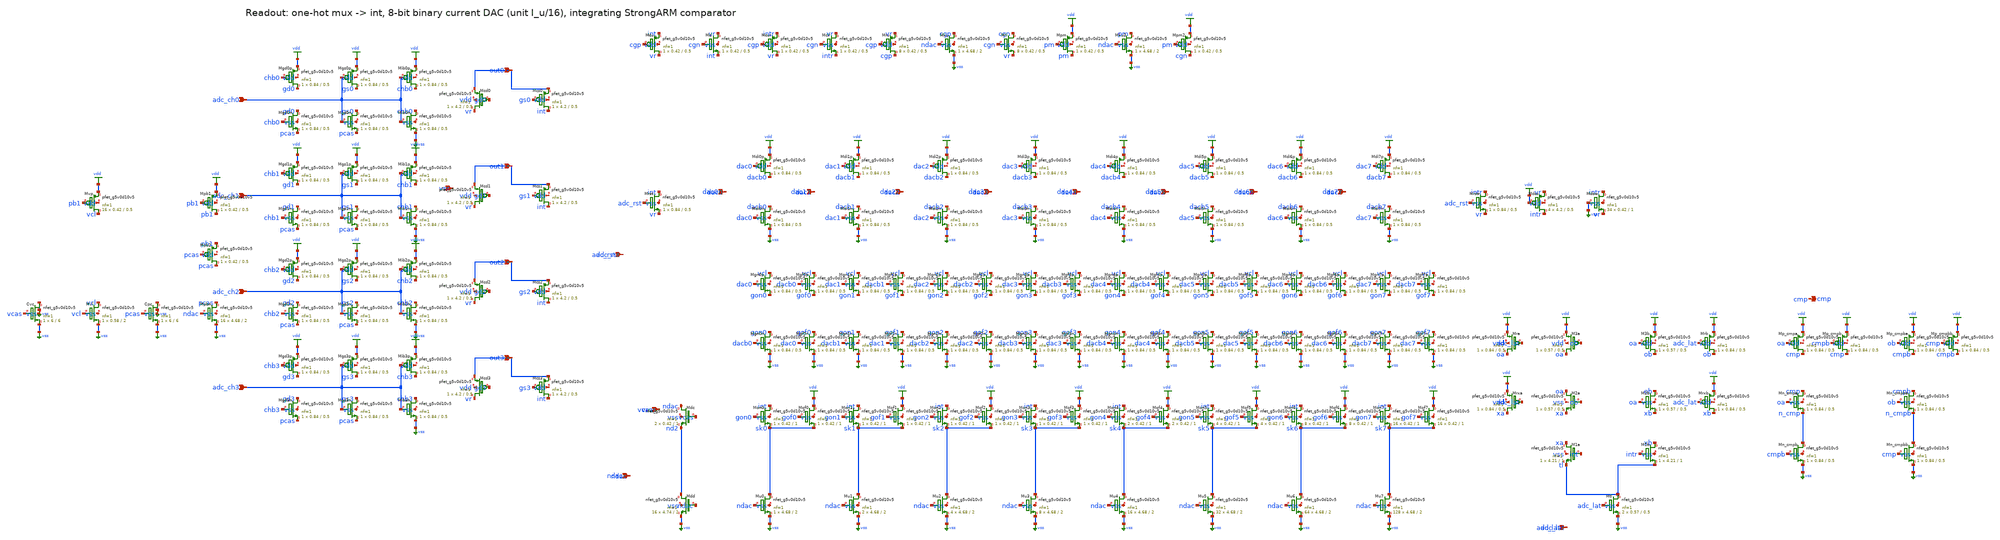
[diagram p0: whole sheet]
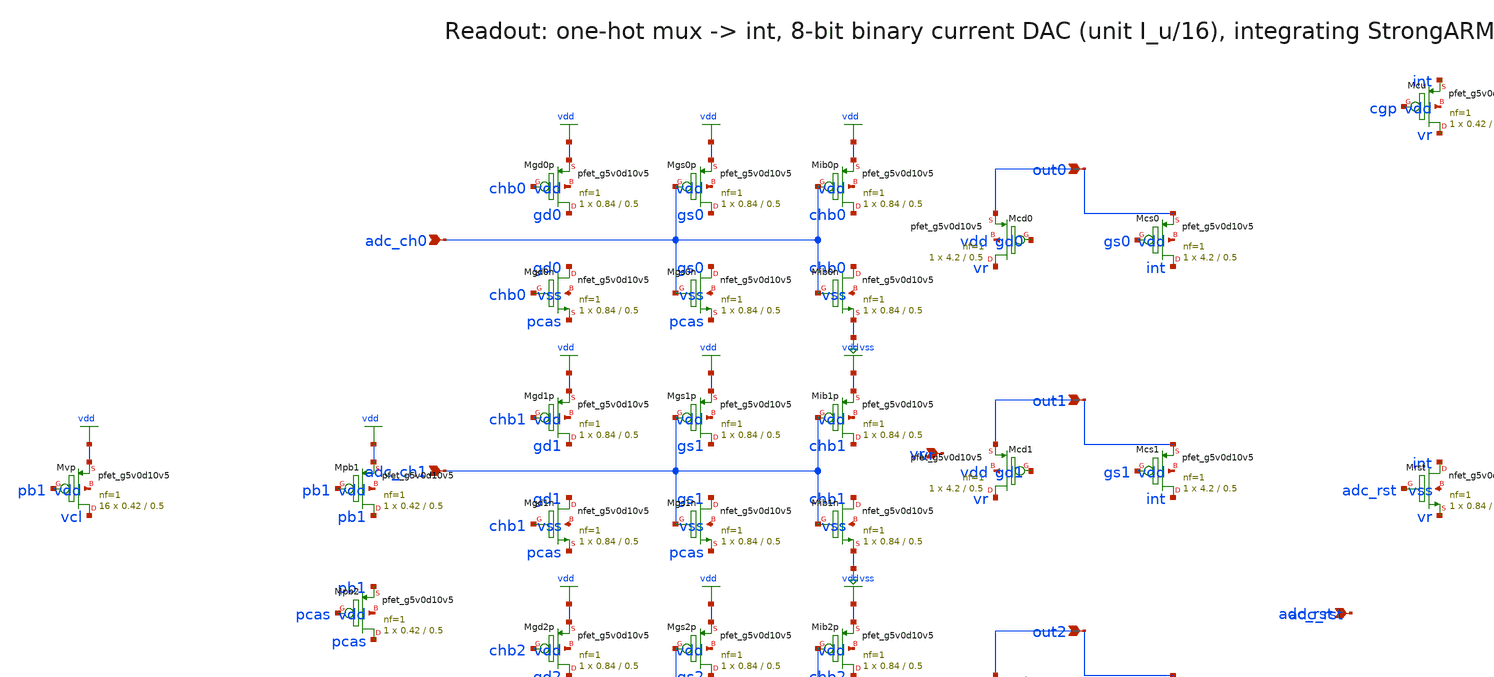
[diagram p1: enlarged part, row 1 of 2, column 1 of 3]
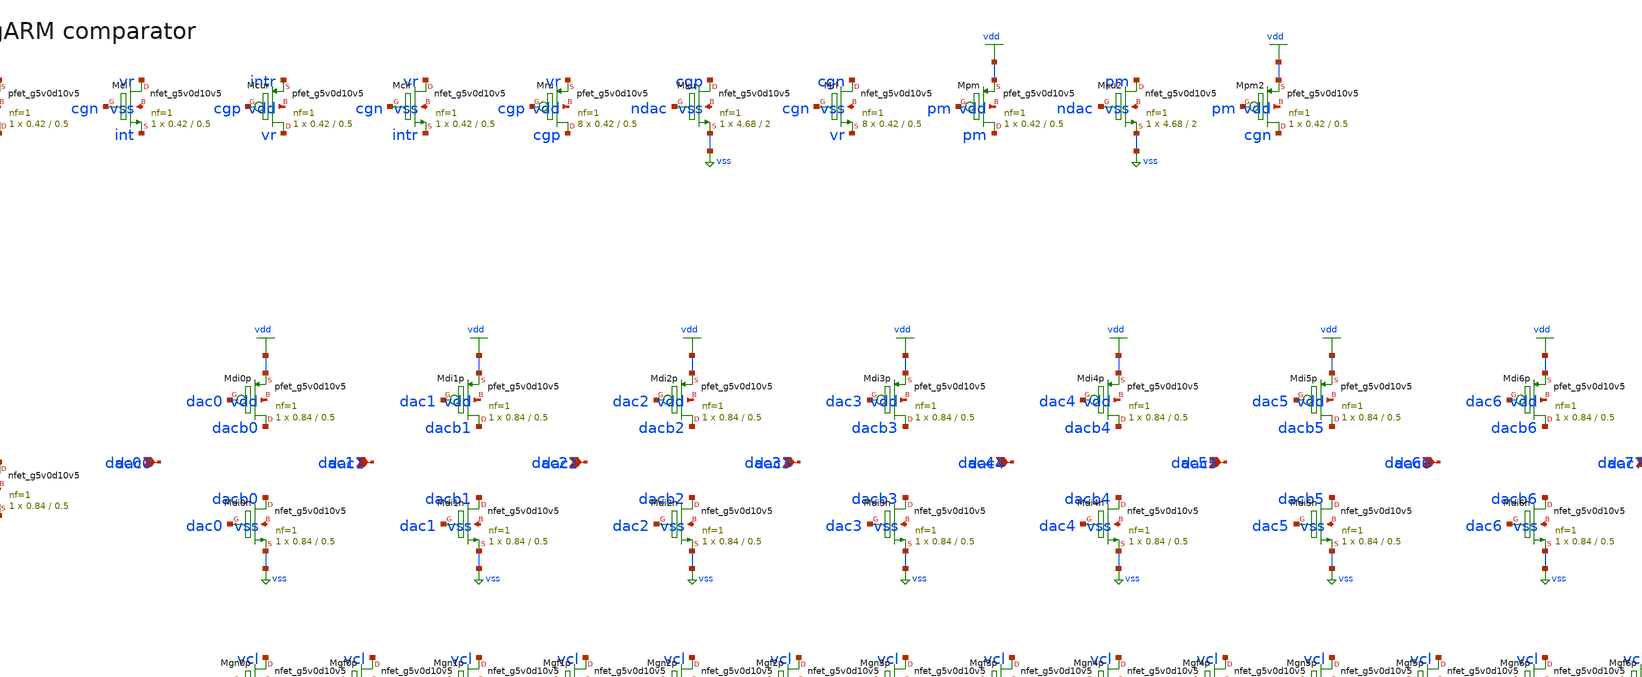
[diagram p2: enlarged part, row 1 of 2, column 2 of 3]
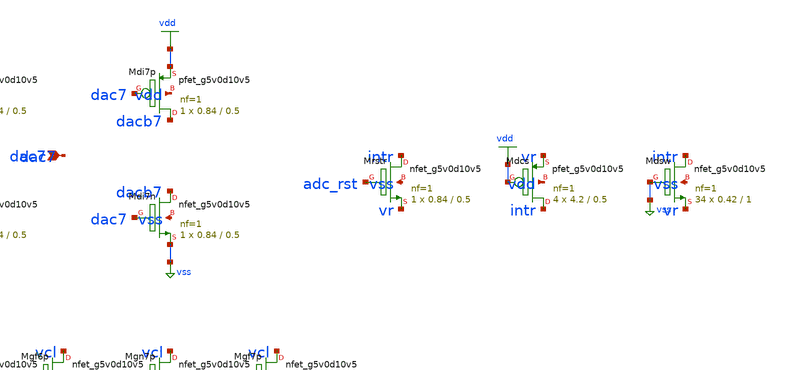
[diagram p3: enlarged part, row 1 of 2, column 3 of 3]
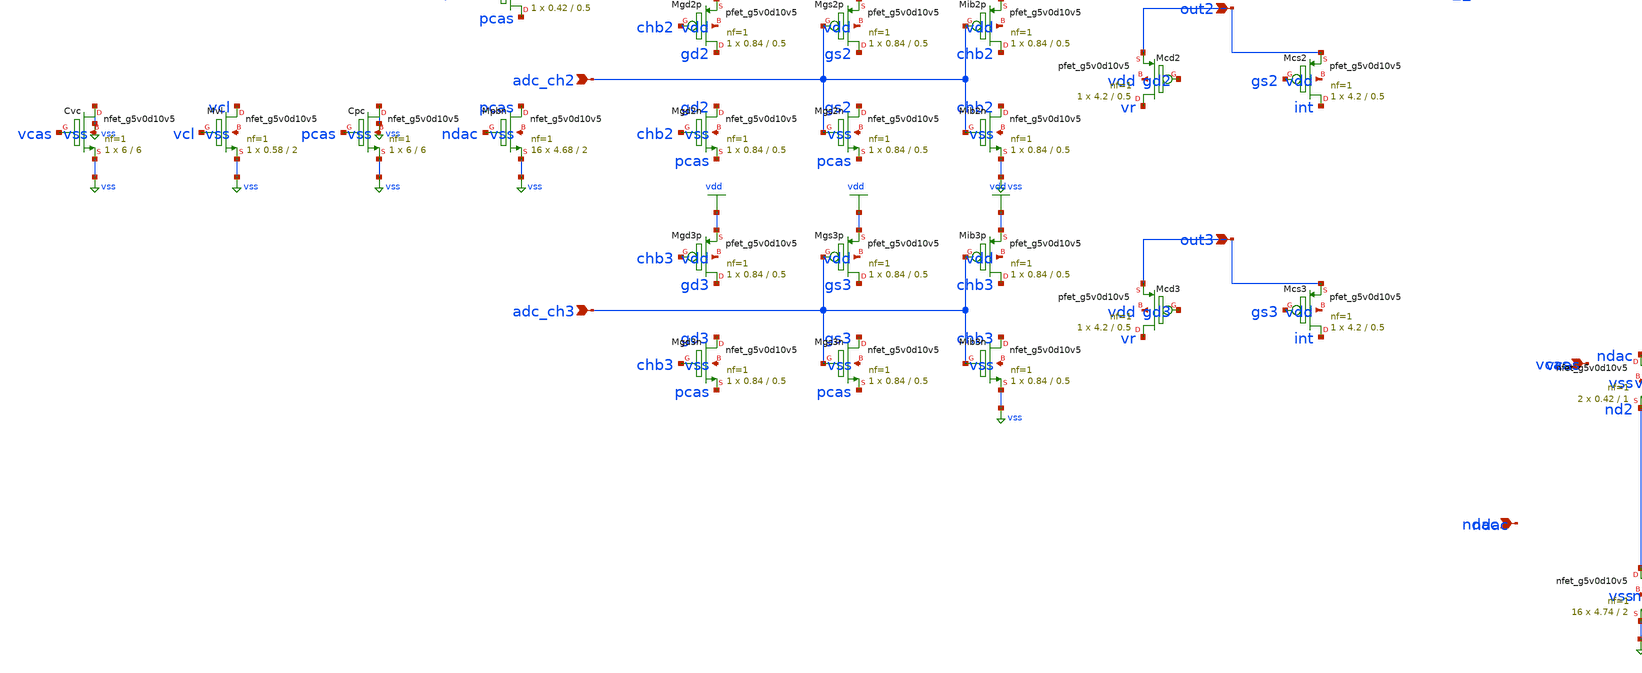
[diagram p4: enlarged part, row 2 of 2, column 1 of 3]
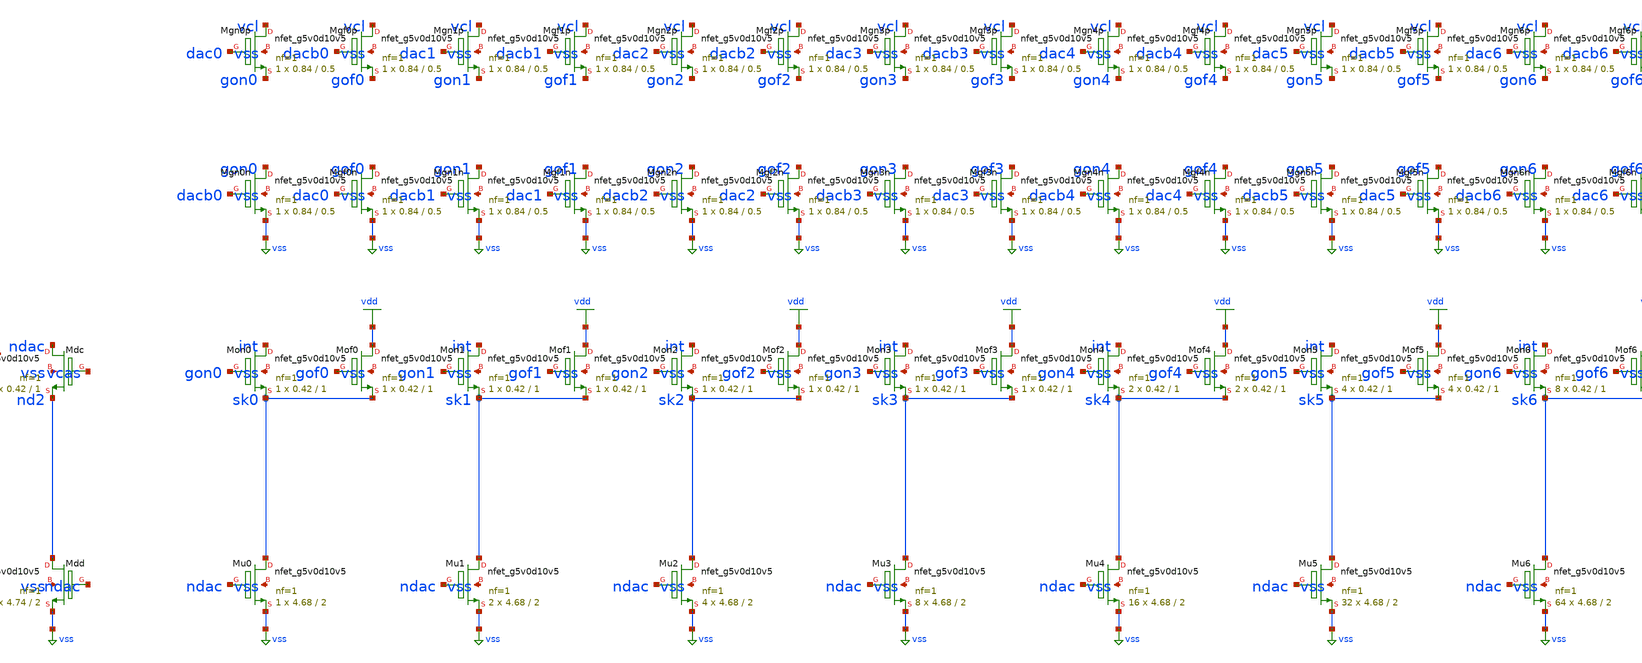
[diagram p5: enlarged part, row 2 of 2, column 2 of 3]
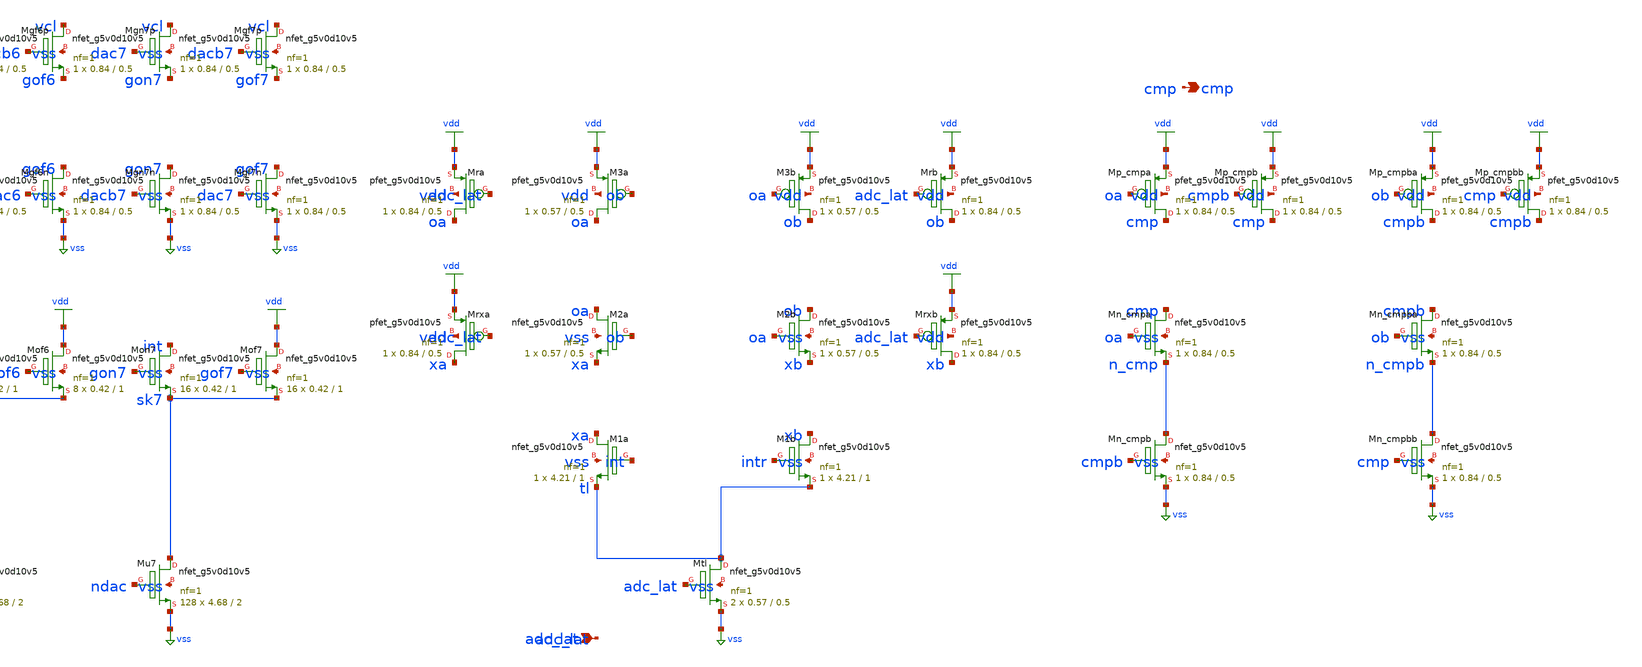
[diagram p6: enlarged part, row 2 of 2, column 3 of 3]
** sch_path: xschem/rt5w_readout.sch
**.subckt rt5w_readout out0 adc_ch0 out1 adc_ch1 out2 adc_ch2 out3 adc_ch3 dac0 dac1 dac2 dac3 dac4
*+ dac5 dac6 dac7 ndac vcas vr adc_rst adc_lat cmp
*.ipin out0
*.ipin adc_ch0
*.ipin out1
*.ipin adc_ch1
*.ipin out2
*.ipin adc_ch2
*.ipin out3
*.ipin adc_ch3
*.ipin dac0
*.ipin dac1
*.ipin dac2
*.ipin dac3
*.ipin dac4
*.ipin dac5
*.ipin dac6
*.ipin dac7
*.ipin ndac
*.ipin vcas
*.ipin vr
*.ipin adc_rst
*.ipin adc_lat
*.opin cmp
XMcs0 int gs0 out0 vdd sky130_fd_pr__pfet_g5v0d10v5 L=0.5 W=4.2 nf=1 ad=1.218 as=1.218 pd=8.98
+ ps=8.98 nrd=0.06905 nrs=0.06905 sa=0 sb=0 sd=0 mult=1 m=1
XMcd0 vr gd0 out0 vdd sky130_fd_pr__pfet_g5v0d10v5 L=0.5 W=4.2 nf=1 ad=1.218 as=1.218 pd=8.98
+ ps=8.98 nrd=0.06905 nrs=0.06905 sa=0 sb=0 sd=0 mult=1 m=1
XMib0p chb0 adc_ch0 vdd vdd sky130_fd_pr__pfet_g5v0d10v5 L=0.5 W=0.84 nf=1 ad=0.2436 as=0.2436
+ pd=2.26 ps=2.26 nrd=0.3452 nrs=0.3452 sa=0 sb=0 sd=0 mult=1 m=1
XMib0n chb0 adc_ch0 vss vss sky130_fd_pr__nfet_g5v0d10v5 L=0.5 W=0.84 nf=1 ad=0.2436 as=0.2436
+ pd=2.26 ps=2.26 nrd=0.3452 nrs=0.3452 sa=0 sb=0 sd=0 mult=1 m=1
XMgs0p gs0 adc_ch0 vdd vdd sky130_fd_pr__pfet_g5v0d10v5 L=0.5 W=0.84 nf=1 ad=0.2436 as=0.2436
+ pd=2.26 ps=2.26 nrd=0.3452 nrs=0.3452 sa=0 sb=0 sd=0 mult=1 m=1
XMgs0n gs0 adc_ch0 pcas vss sky130_fd_pr__nfet_g5v0d10v5 L=0.5 W=0.84 nf=1 ad=0.2436 as=0.2436
+ pd=2.26 ps=2.26 nrd=0.3452 nrs=0.3452 sa=0 sb=0 sd=0 mult=1 m=1
XMgd0p gd0 chb0 vdd vdd sky130_fd_pr__pfet_g5v0d10v5 L=0.5 W=0.84 nf=1 ad=0.2436 as=0.2436 pd=2.26
+ ps=2.26 nrd=0.3452 nrs=0.3452 sa=0 sb=0 sd=0 mult=1 m=1
XMgd0n gd0 chb0 pcas vss sky130_fd_pr__nfet_g5v0d10v5 L=0.5 W=0.84 nf=1 ad=0.2436 as=0.2436 pd=2.26
+ ps=2.26 nrd=0.3452 nrs=0.3452 sa=0 sb=0 sd=0 mult=1 m=1
XMcs1 int gs1 out1 vdd sky130_fd_pr__pfet_g5v0d10v5 L=0.5 W=4.2 nf=1 ad=1.218 as=1.218 pd=8.98
+ ps=8.98 nrd=0.06905 nrs=0.06905 sa=0 sb=0 sd=0 mult=1 m=1
XMcd1 vr gd1 out1 vdd sky130_fd_pr__pfet_g5v0d10v5 L=0.5 W=4.2 nf=1 ad=1.218 as=1.218 pd=8.98
+ ps=8.98 nrd=0.06905 nrs=0.06905 sa=0 sb=0 sd=0 mult=1 m=1
XMib1p chb1 adc_ch1 vdd vdd sky130_fd_pr__pfet_g5v0d10v5 L=0.5 W=0.84 nf=1 ad=0.2436 as=0.2436
+ pd=2.26 ps=2.26 nrd=0.3452 nrs=0.3452 sa=0 sb=0 sd=0 mult=1 m=1
XMib1n chb1 adc_ch1 vss vss sky130_fd_pr__nfet_g5v0d10v5 L=0.5 W=0.84 nf=1 ad=0.2436 as=0.2436
+ pd=2.26 ps=2.26 nrd=0.3452 nrs=0.3452 sa=0 sb=0 sd=0 mult=1 m=1
XMgs1p gs1 adc_ch1 vdd vdd sky130_fd_pr__pfet_g5v0d10v5 L=0.5 W=0.84 nf=1 ad=0.2436 as=0.2436
+ pd=2.26 ps=2.26 nrd=0.3452 nrs=0.3452 sa=0 sb=0 sd=0 mult=1 m=1
XMgs1n gs1 adc_ch1 pcas vss sky130_fd_pr__nfet_g5v0d10v5 L=0.5 W=0.84 nf=1 ad=0.2436 as=0.2436
+ pd=2.26 ps=2.26 nrd=0.3452 nrs=0.3452 sa=0 sb=0 sd=0 mult=1 m=1
XMgd1p gd1 chb1 vdd vdd sky130_fd_pr__pfet_g5v0d10v5 L=0.5 W=0.84 nf=1 ad=0.2436 as=0.2436 pd=2.26
+ ps=2.26 nrd=0.3452 nrs=0.3452 sa=0 sb=0 sd=0 mult=1 m=1
XMgd1n gd1 chb1 pcas vss sky130_fd_pr__nfet_g5v0d10v5 L=0.5 W=0.84 nf=1 ad=0.2436 as=0.2436 pd=2.26
+ ps=2.26 nrd=0.3452 nrs=0.3452 sa=0 sb=0 sd=0 mult=1 m=1
XMcs2 int gs2 out2 vdd sky130_fd_pr__pfet_g5v0d10v5 L=0.5 W=4.2 nf=1 ad=1.218 as=1.218 pd=8.98
+ ps=8.98 nrd=0.06905 nrs=0.06905 sa=0 sb=0 sd=0 mult=1 m=1
XMcd2 vr gd2 out2 vdd sky130_fd_pr__pfet_g5v0d10v5 L=0.5 W=4.2 nf=1 ad=1.218 as=1.218 pd=8.98
+ ps=8.98 nrd=0.06905 nrs=0.06905 sa=0 sb=0 sd=0 mult=1 m=1
XMib2p chb2 adc_ch2 vdd vdd sky130_fd_pr__pfet_g5v0d10v5 L=0.5 W=0.84 nf=1 ad=0.2436 as=0.2436
+ pd=2.26 ps=2.26 nrd=0.3452 nrs=0.3452 sa=0 sb=0 sd=0 mult=1 m=1
XMib2n chb2 adc_ch2 vss vss sky130_fd_pr__nfet_g5v0d10v5 L=0.5 W=0.84 nf=1 ad=0.2436 as=0.2436
+ pd=2.26 ps=2.26 nrd=0.3452 nrs=0.3452 sa=0 sb=0 sd=0 mult=1 m=1
XMgs2p gs2 adc_ch2 vdd vdd sky130_fd_pr__pfet_g5v0d10v5 L=0.5 W=0.84 nf=1 ad=0.2436 as=0.2436
+ pd=2.26 ps=2.26 nrd=0.3452 nrs=0.3452 sa=0 sb=0 sd=0 mult=1 m=1
XMgs2n gs2 adc_ch2 pcas vss sky130_fd_pr__nfet_g5v0d10v5 L=0.5 W=0.84 nf=1 ad=0.2436 as=0.2436
+ pd=2.26 ps=2.26 nrd=0.3452 nrs=0.3452 sa=0 sb=0 sd=0 mult=1 m=1
XMgd2p gd2 chb2 vdd vdd sky130_fd_pr__pfet_g5v0d10v5 L=0.5 W=0.84 nf=1 ad=0.2436 as=0.2436 pd=2.26
+ ps=2.26 nrd=0.3452 nrs=0.3452 sa=0 sb=0 sd=0 mult=1 m=1
XMgd2n gd2 chb2 pcas vss sky130_fd_pr__nfet_g5v0d10v5 L=0.5 W=0.84 nf=1 ad=0.2436 as=0.2436 pd=2.26
+ ps=2.26 nrd=0.3452 nrs=0.3452 sa=0 sb=0 sd=0 mult=1 m=1
XMcs3 int gs3 out3 vdd sky130_fd_pr__pfet_g5v0d10v5 L=0.5 W=4.2 nf=1 ad=1.218 as=1.218 pd=8.98
+ ps=8.98 nrd=0.06905 nrs=0.06905 sa=0 sb=0 sd=0 mult=1 m=1
XMcd3 vr gd3 out3 vdd sky130_fd_pr__pfet_g5v0d10v5 L=0.5 W=4.2 nf=1 ad=1.218 as=1.218 pd=8.98
+ ps=8.98 nrd=0.06905 nrs=0.06905 sa=0 sb=0 sd=0 mult=1 m=1
XMib3p chb3 adc_ch3 vdd vdd sky130_fd_pr__pfet_g5v0d10v5 L=0.5 W=0.84 nf=1 ad=0.2436 as=0.2436
+ pd=2.26 ps=2.26 nrd=0.3452 nrs=0.3452 sa=0 sb=0 sd=0 mult=1 m=1
XMib3n chb3 adc_ch3 vss vss sky130_fd_pr__nfet_g5v0d10v5 L=0.5 W=0.84 nf=1 ad=0.2436 as=0.2436
+ pd=2.26 ps=2.26 nrd=0.3452 nrs=0.3452 sa=0 sb=0 sd=0 mult=1 m=1
XMgs3p gs3 adc_ch3 vdd vdd sky130_fd_pr__pfet_g5v0d10v5 L=0.5 W=0.84 nf=1 ad=0.2436 as=0.2436
+ pd=2.26 ps=2.26 nrd=0.3452 nrs=0.3452 sa=0 sb=0 sd=0 mult=1 m=1
XMgs3n gs3 adc_ch3 pcas vss sky130_fd_pr__nfet_g5v0d10v5 L=0.5 W=0.84 nf=1 ad=0.2436 as=0.2436
+ pd=2.26 ps=2.26 nrd=0.3452 nrs=0.3452 sa=0 sb=0 sd=0 mult=1 m=1
XMgd3p gd3 chb3 vdd vdd sky130_fd_pr__pfet_g5v0d10v5 L=0.5 W=0.84 nf=1 ad=0.2436 as=0.2436 pd=2.26
+ ps=2.26 nrd=0.3452 nrs=0.3452 sa=0 sb=0 sd=0 mult=1 m=1
XMgd3n gd3 chb3 pcas vss sky130_fd_pr__nfet_g5v0d10v5 L=0.5 W=0.84 nf=1 ad=0.2436 as=0.2436 pd=2.26
+ ps=2.26 nrd=0.3452 nrs=0.3452 sa=0 sb=0 sd=0 mult=1 m=1
XMpb1 pb1 pb1 vdd vdd sky130_fd_pr__pfet_g5v0d10v5 L=0.5 W=0.42 nf=1 ad=0.1218 as=0.1218 pd=1.42
+ ps=1.42 nrd=0.6905 nrs=0.6905 sa=0 sb=0 sd=0 mult=1 m=1
XMpb2 pcas pcas pb1 vdd sky130_fd_pr__pfet_g5v0d10v5 L=0.5 W=0.42 nf=1 ad=0.1218 as=0.1218 pd=1.42
+ ps=1.42 nrd=0.6905 nrs=0.6905 sa=0 sb=0 sd=0 mult=1 m=1
XMpbn pcas ndac vss vss sky130_fd_pr__nfet_g5v0d10v5 L=2 W=4.68 nf=1 ad=1.357 as=1.357 pd=9.94
+ ps=9.94 nrd=0.06197 nrs=0.06197 sa=0 sb=0 sd=0 mult=16 m=16
XCpc vss pcas vss vss sky130_fd_pr__nfet_g5v0d10v5 L=6 W=6 nf=1 ad=1.74 as=1.74 pd=12.58 ps=12.58
+ nrd=0.04833 nrs=0.04833 sa=0 sb=0 sd=0 mult=1 m=1
XMvp vcl pb1 vdd vdd sky130_fd_pr__pfet_g5v0d10v5 L=0.5 W=0.42 nf=1 ad=0.1218 as=0.1218 pd=1.42
+ ps=1.42 nrd=0.6905 nrs=0.6905 sa=0 sb=0 sd=0 mult=16 m=16
XMvl vcl vcl vss vss sky130_fd_pr__nfet_g5v0d10v5 L=2 W=0.58 nf=1 ad=0.1682 as=0.1682 pd=1.74
+ ps=1.74 nrd=0.5 nrs=0.5 sa=0 sb=0 sd=0 mult=1 m=1
XCvc vss vcas vss vss sky130_fd_pr__nfet_g5v0d10v5 L=6 W=6 nf=1 ad=1.74 as=1.74 pd=12.58 ps=12.58
+ nrd=0.04833 nrs=0.04833 sa=0 sb=0 sd=0 mult=1 m=1
XMrst int adc_rst vr vss sky130_fd_pr__nfet_g5v0d10v5 L=0.5 W=0.84 nf=1 ad=0.2436 as=0.2436 pd=2.26
+ ps=2.26 nrd=0.3452 nrs=0.3452 sa=0 sb=0 sd=0 mult=1 m=1
XMcu vr cgp int vdd sky130_fd_pr__pfet_g5v0d10v5 L=0.5 W=0.42 nf=1 ad=0.1218 as=0.1218 pd=1.42
+ ps=1.42 nrd=0.6905 nrs=0.6905 sa=0 sb=0 sd=0 mult=1 m=1
XMcl vr cgn int vss sky130_fd_pr__nfet_g5v0d10v5 L=0.5 W=0.42 nf=1 ad=0.1218 as=0.1218 pd=1.42
+ ps=1.42 nrd=0.6905 nrs=0.6905 sa=0 sb=0 sd=0 mult=1 m=1
XMcur vr cgp intr vdd sky130_fd_pr__pfet_g5v0d10v5 L=0.5 W=0.42 nf=1 ad=0.1218 as=0.1218 pd=1.42
+ ps=1.42 nrd=0.6905 nrs=0.6905 sa=0 sb=0 sd=0 mult=1 m=1
XMclr vr cgn intr vss sky130_fd_pr__nfet_g5v0d10v5 L=0.5 W=0.42 nf=1 ad=0.1218 as=0.1218 pd=1.42
+ ps=1.42 nrd=0.6905 nrs=0.6905 sa=0 sb=0 sd=0 mult=1 m=1
XMru cgp cgp vr vdd sky130_fd_pr__pfet_g5v0d10v5 L=0.5 W=0.42 nf=1 ad=0.1218 as=0.1218 pd=1.42
+ ps=1.42 nrd=0.6905 nrs=0.6905 sa=0 sb=0 sd=0 mult=8 m=8
XMku cgp ndac vss vss sky130_fd_pr__nfet_g5v0d10v5 L=2 W=4.68 nf=1 ad=1.357 as=1.357 pd=9.94 ps=9.94
+ nrd=0.06197 nrs=0.06197 sa=0 sb=0 sd=0 mult=1 m=1
XMrl cgn cgn vr vss sky130_fd_pr__nfet_g5v0d10v5 L=0.5 W=0.42 nf=1 ad=0.1218 as=0.1218 pd=1.42
+ ps=1.42 nrd=0.6905 nrs=0.6905 sa=0 sb=0 sd=0 mult=8 m=8
XMpm pm pm vdd vdd sky130_fd_pr__pfet_g5v0d10v5 L=0.5 W=0.42 nf=1 ad=0.1218 as=0.1218 pd=1.42
+ ps=1.42 nrd=0.6905 nrs=0.6905 sa=0 sb=0 sd=0 mult=1 m=1
XMku2 pm ndac vss vss sky130_fd_pr__nfet_g5v0d10v5 L=2 W=4.68 nf=1 ad=1.357 as=1.357 pd=9.94 ps=9.94
+ nrd=0.06197 nrs=0.06197 sa=0 sb=0 sd=0 mult=1 m=1
XMpm2 cgn pm vdd vdd sky130_fd_pr__pfet_g5v0d10v5 L=0.5 W=0.42 nf=1 ad=0.1218 as=0.1218 pd=1.42
+ ps=1.42 nrd=0.6905 nrs=0.6905 sa=0 sb=0 sd=0 mult=1 m=1
XMrstr intr adc_rst vr vss sky130_fd_pr__nfet_g5v0d10v5 L=0.5 W=0.84 nf=1 ad=0.2436 as=0.2436
+ pd=2.26 ps=2.26 nrd=0.3452 nrs=0.3452 sa=0 sb=0 sd=0 mult=1 m=1
XMdcs intr vdd vr vdd sky130_fd_pr__pfet_g5v0d10v5 L=0.5 W=4.2 nf=1 ad=1.218 as=1.218 pd=8.98
+ ps=8.98 nrd=0.06905 nrs=0.06905 sa=0 sb=0 sd=0 mult=4 m=4
XMdsw intr vss vr vss sky130_fd_pr__nfet_g5v0d10v5 L=1 W=0.42 nf=1 ad=0.1218 as=0.1218 pd=1.42
+ ps=1.42 nrd=0.6905 nrs=0.6905 sa=0 sb=0 sd=0 mult=34 m=34
XMdc ndac vcas nd2 vss sky130_fd_pr__nfet_g5v0d10v5 L=1 W=0.42 nf=1 ad=0.1218 as=0.1218 pd=1.42
+ ps=1.42 nrd=0.6905 nrs=0.6905 sa=0 sb=0 sd=0 mult=2 m=2
XMdd nd2 ndac vss vss sky130_fd_pr__nfet_g5v0d10v5 L=2 W=4.74 nf=1 ad=1.375 as=1.375 pd=10.06
+ ps=10.06 nrd=0.06118 nrs=0.06118 sa=0 sb=0 sd=0 mult=16 m=16
XMdi0p dacb0 dac0 vdd vdd sky130_fd_pr__pfet_g5v0d10v5 L=0.5 W=0.84 nf=1 ad=0.2436 as=0.2436 pd=2.26
+ ps=2.26 nrd=0.3452 nrs=0.3452 sa=0 sb=0 sd=0 mult=1 m=1
XMdi0n dacb0 dac0 vss vss sky130_fd_pr__nfet_g5v0d10v5 L=0.5 W=0.84 nf=1 ad=0.2436 as=0.2436 pd=2.26
+ ps=2.26 nrd=0.3452 nrs=0.3452 sa=0 sb=0 sd=0 mult=1 m=1
XMon0 int gon0 sk0 vss sky130_fd_pr__nfet_g5v0d10v5 L=1 W=0.42 nf=1 ad=0.1218 as=0.1218 pd=1.42
+ ps=1.42 nrd=0.6905 nrs=0.6905 sa=0 sb=0 sd=0 mult=1 m=1
XMof0 vdd gof0 sk0 vss sky130_fd_pr__nfet_g5v0d10v5 L=1 W=0.42 nf=1 ad=0.1218 as=0.1218 pd=1.42
+ ps=1.42 nrd=0.6905 nrs=0.6905 sa=0 sb=0 sd=0 mult=1 m=1
XMgn0p vcl dac0 gon0 vss sky130_fd_pr__nfet_g5v0d10v5 L=0.5 W=0.84 nf=1 ad=0.2436 as=0.2436 pd=2.26
+ ps=2.26 nrd=0.3452 nrs=0.3452 sa=0 sb=0 sd=0 mult=1 m=1
XMgn0n gon0 dacb0 vss vss sky130_fd_pr__nfet_g5v0d10v5 L=0.5 W=0.84 nf=1 ad=0.2436 as=0.2436 pd=2.26
+ ps=2.26 nrd=0.3452 nrs=0.3452 sa=0 sb=0 sd=0 mult=1 m=1
XMgf0p vcl dacb0 gof0 vss sky130_fd_pr__nfet_g5v0d10v5 L=0.5 W=0.84 nf=1 ad=0.2436 as=0.2436 pd=2.26
+ ps=2.26 nrd=0.3452 nrs=0.3452 sa=0 sb=0 sd=0 mult=1 m=1
XMgf0n gof0 dac0 vss vss sky130_fd_pr__nfet_g5v0d10v5 L=0.5 W=0.84 nf=1 ad=0.2436 as=0.2436 pd=2.26
+ ps=2.26 nrd=0.3452 nrs=0.3452 sa=0 sb=0 sd=0 mult=1 m=1
XMu0 sk0 ndac vss vss sky130_fd_pr__nfet_g5v0d10v5 L=2 W=4.68 nf=1 ad=1.357 as=1.357 pd=9.94 ps=9.94
+ nrd=0.06197 nrs=0.06197 sa=0 sb=0 sd=0 mult=1 m=1
XMdi1p dacb1 dac1 vdd vdd sky130_fd_pr__pfet_g5v0d10v5 L=0.5 W=0.84 nf=1 ad=0.2436 as=0.2436 pd=2.26
+ ps=2.26 nrd=0.3452 nrs=0.3452 sa=0 sb=0 sd=0 mult=1 m=1
XMdi1n dacb1 dac1 vss vss sky130_fd_pr__nfet_g5v0d10v5 L=0.5 W=0.84 nf=1 ad=0.2436 as=0.2436 pd=2.26
+ ps=2.26 nrd=0.3452 nrs=0.3452 sa=0 sb=0 sd=0 mult=1 m=1
XMon1 int gon1 sk1 vss sky130_fd_pr__nfet_g5v0d10v5 L=1 W=0.42 nf=1 ad=0.1218 as=0.1218 pd=1.42
+ ps=1.42 nrd=0.6905 nrs=0.6905 sa=0 sb=0 sd=0 mult=1 m=1
XMof1 vdd gof1 sk1 vss sky130_fd_pr__nfet_g5v0d10v5 L=1 W=0.42 nf=1 ad=0.1218 as=0.1218 pd=1.42
+ ps=1.42 nrd=0.6905 nrs=0.6905 sa=0 sb=0 sd=0 mult=1 m=1
XMgn1p vcl dac1 gon1 vss sky130_fd_pr__nfet_g5v0d10v5 L=0.5 W=0.84 nf=1 ad=0.2436 as=0.2436 pd=2.26
+ ps=2.26 nrd=0.3452 nrs=0.3452 sa=0 sb=0 sd=0 mult=1 m=1
XMgn1n gon1 dacb1 vss vss sky130_fd_pr__nfet_g5v0d10v5 L=0.5 W=0.84 nf=1 ad=0.2436 as=0.2436 pd=2.26
+ ps=2.26 nrd=0.3452 nrs=0.3452 sa=0 sb=0 sd=0 mult=1 m=1
XMgf1p vcl dacb1 gof1 vss sky130_fd_pr__nfet_g5v0d10v5 L=0.5 W=0.84 nf=1 ad=0.2436 as=0.2436 pd=2.26
+ ps=2.26 nrd=0.3452 nrs=0.3452 sa=0 sb=0 sd=0 mult=1 m=1
XMgf1n gof1 dac1 vss vss sky130_fd_pr__nfet_g5v0d10v5 L=0.5 W=0.84 nf=1 ad=0.2436 as=0.2436 pd=2.26
+ ps=2.26 nrd=0.3452 nrs=0.3452 sa=0 sb=0 sd=0 mult=1 m=1
XMu1 sk1 ndac vss vss sky130_fd_pr__nfet_g5v0d10v5 L=2 W=4.68 nf=1 ad=1.357 as=1.357 pd=9.94 ps=9.94
+ nrd=0.06197 nrs=0.06197 sa=0 sb=0 sd=0 mult=2 m=2
XMdi2p dacb2 dac2 vdd vdd sky130_fd_pr__pfet_g5v0d10v5 L=0.5 W=0.84 nf=1 ad=0.2436 as=0.2436 pd=2.26
+ ps=2.26 nrd=0.3452 nrs=0.3452 sa=0 sb=0 sd=0 mult=1 m=1
XMdi2n dacb2 dac2 vss vss sky130_fd_pr__nfet_g5v0d10v5 L=0.5 W=0.84 nf=1 ad=0.2436 as=0.2436 pd=2.26
+ ps=2.26 nrd=0.3452 nrs=0.3452 sa=0 sb=0 sd=0 mult=1 m=1
XMon2 int gon2 sk2 vss sky130_fd_pr__nfet_g5v0d10v5 L=1 W=0.42 nf=1 ad=0.1218 as=0.1218 pd=1.42
+ ps=1.42 nrd=0.6905 nrs=0.6905 sa=0 sb=0 sd=0 mult=1 m=1
XMof2 vdd gof2 sk2 vss sky130_fd_pr__nfet_g5v0d10v5 L=1 W=0.42 nf=1 ad=0.1218 as=0.1218 pd=1.42
+ ps=1.42 nrd=0.6905 nrs=0.6905 sa=0 sb=0 sd=0 mult=1 m=1
XMgn2p vcl dac2 gon2 vss sky130_fd_pr__nfet_g5v0d10v5 L=0.5 W=0.84 nf=1 ad=0.2436 as=0.2436 pd=2.26
+ ps=2.26 nrd=0.3452 nrs=0.3452 sa=0 sb=0 sd=0 mult=1 m=1
XMgn2n gon2 dacb2 vss vss sky130_fd_pr__nfet_g5v0d10v5 L=0.5 W=0.84 nf=1 ad=0.2436 as=0.2436 pd=2.26
+ ps=2.26 nrd=0.3452 nrs=0.3452 sa=0 sb=0 sd=0 mult=1 m=1
XMgf2p vcl dacb2 gof2 vss sky130_fd_pr__nfet_g5v0d10v5 L=0.5 W=0.84 nf=1 ad=0.2436 as=0.2436 pd=2.26
+ ps=2.26 nrd=0.3452 nrs=0.3452 sa=0 sb=0 sd=0 mult=1 m=1
XMgf2n gof2 dac2 vss vss sky130_fd_pr__nfet_g5v0d10v5 L=0.5 W=0.84 nf=1 ad=0.2436 as=0.2436 pd=2.26
+ ps=2.26 nrd=0.3452 nrs=0.3452 sa=0 sb=0 sd=0 mult=1 m=1
XMu2 sk2 ndac vss vss sky130_fd_pr__nfet_g5v0d10v5 L=2 W=4.68 nf=1 ad=1.357 as=1.357 pd=9.94 ps=9.94
+ nrd=0.06197 nrs=0.06197 sa=0 sb=0 sd=0 mult=4 m=4
XMdi3p dacb3 dac3 vdd vdd sky130_fd_pr__pfet_g5v0d10v5 L=0.5 W=0.84 nf=1 ad=0.2436 as=0.2436 pd=2.26
+ ps=2.26 nrd=0.3452 nrs=0.3452 sa=0 sb=0 sd=0 mult=1 m=1
XMdi3n dacb3 dac3 vss vss sky130_fd_pr__nfet_g5v0d10v5 L=0.5 W=0.84 nf=1 ad=0.2436 as=0.2436 pd=2.26
+ ps=2.26 nrd=0.3452 nrs=0.3452 sa=0 sb=0 sd=0 mult=1 m=1
XMon3 int gon3 sk3 vss sky130_fd_pr__nfet_g5v0d10v5 L=1 W=0.42 nf=1 ad=0.1218 as=0.1218 pd=1.42
+ ps=1.42 nrd=0.6905 nrs=0.6905 sa=0 sb=0 sd=0 mult=1 m=1
XMof3 vdd gof3 sk3 vss sky130_fd_pr__nfet_g5v0d10v5 L=1 W=0.42 nf=1 ad=0.1218 as=0.1218 pd=1.42
+ ps=1.42 nrd=0.6905 nrs=0.6905 sa=0 sb=0 sd=0 mult=1 m=1
XMgn3p vcl dac3 gon3 vss sky130_fd_pr__nfet_g5v0d10v5 L=0.5 W=0.84 nf=1 ad=0.2436 as=0.2436 pd=2.26
+ ps=2.26 nrd=0.3452 nrs=0.3452 sa=0 sb=0 sd=0 mult=1 m=1
XMgn3n gon3 dacb3 vss vss sky130_fd_pr__nfet_g5v0d10v5 L=0.5 W=0.84 nf=1 ad=0.2436 as=0.2436 pd=2.26
+ ps=2.26 nrd=0.3452 nrs=0.3452 sa=0 sb=0 sd=0 mult=1 m=1
XMgf3p vcl dacb3 gof3 vss sky130_fd_pr__nfet_g5v0d10v5 L=0.5 W=0.84 nf=1 ad=0.2436 as=0.2436 pd=2.26
+ ps=2.26 nrd=0.3452 nrs=0.3452 sa=0 sb=0 sd=0 mult=1 m=1
XMgf3n gof3 dac3 vss vss sky130_fd_pr__nfet_g5v0d10v5 L=0.5 W=0.84 nf=1 ad=0.2436 as=0.2436 pd=2.26
+ ps=2.26 nrd=0.3452 nrs=0.3452 sa=0 sb=0 sd=0 mult=1 m=1
XMu3 sk3 ndac vss vss sky130_fd_pr__nfet_g5v0d10v5 L=2 W=4.68 nf=1 ad=1.357 as=1.357 pd=9.94 ps=9.94
+ nrd=0.06197 nrs=0.06197 sa=0 sb=0 sd=0 mult=8 m=8
XMdi4p dacb4 dac4 vdd vdd sky130_fd_pr__pfet_g5v0d10v5 L=0.5 W=0.84 nf=1 ad=0.2436 as=0.2436 pd=2.26
+ ps=2.26 nrd=0.3452 nrs=0.3452 sa=0 sb=0 sd=0 mult=1 m=1
XMdi4n dacb4 dac4 vss vss sky130_fd_pr__nfet_g5v0d10v5 L=0.5 W=0.84 nf=1 ad=0.2436 as=0.2436 pd=2.26
+ ps=2.26 nrd=0.3452 nrs=0.3452 sa=0 sb=0 sd=0 mult=1 m=1
XMon4 int gon4 sk4 vss sky130_fd_pr__nfet_g5v0d10v5 L=1 W=0.42 nf=1 ad=0.1218 as=0.1218 pd=1.42
+ ps=1.42 nrd=0.6905 nrs=0.6905 sa=0 sb=0 sd=0 mult=2 m=2
XMof4 vdd gof4 sk4 vss sky130_fd_pr__nfet_g5v0d10v5 L=1 W=0.42 nf=1 ad=0.1218 as=0.1218 pd=1.42
+ ps=1.42 nrd=0.6905 nrs=0.6905 sa=0 sb=0 sd=0 mult=2 m=2
XMgn4p vcl dac4 gon4 vss sky130_fd_pr__nfet_g5v0d10v5 L=0.5 W=0.84 nf=1 ad=0.2436 as=0.2436 pd=2.26
+ ps=2.26 nrd=0.3452 nrs=0.3452 sa=0 sb=0 sd=0 mult=1 m=1
XMgn4n gon4 dacb4 vss vss sky130_fd_pr__nfet_g5v0d10v5 L=0.5 W=0.84 nf=1 ad=0.2436 as=0.2436 pd=2.26
+ ps=2.26 nrd=0.3452 nrs=0.3452 sa=0 sb=0 sd=0 mult=1 m=1
XMgf4p vcl dacb4 gof4 vss sky130_fd_pr__nfet_g5v0d10v5 L=0.5 W=0.84 nf=1 ad=0.2436 as=0.2436 pd=2.26
+ ps=2.26 nrd=0.3452 nrs=0.3452 sa=0 sb=0 sd=0 mult=1 m=1
XMgf4n gof4 dac4 vss vss sky130_fd_pr__nfet_g5v0d10v5 L=0.5 W=0.84 nf=1 ad=0.2436 as=0.2436 pd=2.26
+ ps=2.26 nrd=0.3452 nrs=0.3452 sa=0 sb=0 sd=0 mult=1 m=1
XMu4 sk4 ndac vss vss sky130_fd_pr__nfet_g5v0d10v5 L=2 W=4.68 nf=1 ad=1.357 as=1.357 pd=9.94 ps=9.94
+ nrd=0.06197 nrs=0.06197 sa=0 sb=0 sd=0 mult=16 m=16
XMdi5p dacb5 dac5 vdd vdd sky130_fd_pr__pfet_g5v0d10v5 L=0.5 W=0.84 nf=1 ad=0.2436 as=0.2436 pd=2.26
+ ps=2.26 nrd=0.3452 nrs=0.3452 sa=0 sb=0 sd=0 mult=1 m=1
XMdi5n dacb5 dac5 vss vss sky130_fd_pr__nfet_g5v0d10v5 L=0.5 W=0.84 nf=1 ad=0.2436 as=0.2436 pd=2.26
+ ps=2.26 nrd=0.3452 nrs=0.3452 sa=0 sb=0 sd=0 mult=1 m=1
XMon5 int gon5 sk5 vss sky130_fd_pr__nfet_g5v0d10v5 L=1 W=0.42 nf=1 ad=0.1218 as=0.1218 pd=1.42
+ ps=1.42 nrd=0.6905 nrs=0.6905 sa=0 sb=0 sd=0 mult=4 m=4
XMof5 vdd gof5 sk5 vss sky130_fd_pr__nfet_g5v0d10v5 L=1 W=0.42 nf=1 ad=0.1218 as=0.1218 pd=1.42
+ ps=1.42 nrd=0.6905 nrs=0.6905 sa=0 sb=0 sd=0 mult=4 m=4
XMgn5p vcl dac5 gon5 vss sky130_fd_pr__nfet_g5v0d10v5 L=0.5 W=0.84 nf=1 ad=0.2436 as=0.2436 pd=2.26
+ ps=2.26 nrd=0.3452 nrs=0.3452 sa=0 sb=0 sd=0 mult=1 m=1
XMgn5n gon5 dacb5 vss vss sky130_fd_pr__nfet_g5v0d10v5 L=0.5 W=0.84 nf=1 ad=0.2436 as=0.2436 pd=2.26
+ ps=2.26 nrd=0.3452 nrs=0.3452 sa=0 sb=0 sd=0 mult=1 m=1
XMgf5p vcl dacb5 gof5 vss sky130_fd_pr__nfet_g5v0d10v5 L=0.5 W=0.84 nf=1 ad=0.2436 as=0.2436 pd=2.26
+ ps=2.26 nrd=0.3452 nrs=0.3452 sa=0 sb=0 sd=0 mult=1 m=1
XMgf5n gof5 dac5 vss vss sky130_fd_pr__nfet_g5v0d10v5 L=0.5 W=0.84 nf=1 ad=0.2436 as=0.2436 pd=2.26
+ ps=2.26 nrd=0.3452 nrs=0.3452 sa=0 sb=0 sd=0 mult=1 m=1
XMu5 sk5 ndac vss vss sky130_fd_pr__nfet_g5v0d10v5 L=2 W=4.68 nf=1 ad=1.357 as=1.357 pd=9.94 ps=9.94
+ nrd=0.06197 nrs=0.06197 sa=0 sb=0 sd=0 mult=32 m=32
XMdi6p dacb6 dac6 vdd vdd sky130_fd_pr__pfet_g5v0d10v5 L=0.5 W=0.84 nf=1 ad=0.2436 as=0.2436 pd=2.26
+ ps=2.26 nrd=0.3452 nrs=0.3452 sa=0 sb=0 sd=0 mult=1 m=1
XMdi6n dacb6 dac6 vss vss sky130_fd_pr__nfet_g5v0d10v5 L=0.5 W=0.84 nf=1 ad=0.2436 as=0.2436 pd=2.26
+ ps=2.26 nrd=0.3452 nrs=0.3452 sa=0 sb=0 sd=0 mult=1 m=1
XMon6 int gon6 sk6 vss sky130_fd_pr__nfet_g5v0d10v5 L=1 W=0.42 nf=1 ad=0.1218 as=0.1218 pd=1.42
+ ps=1.42 nrd=0.6905 nrs=0.6905 sa=0 sb=0 sd=0 mult=8 m=8
XMof6 vdd gof6 sk6 vss sky130_fd_pr__nfet_g5v0d10v5 L=1 W=0.42 nf=1 ad=0.1218 as=0.1218 pd=1.42
+ ps=1.42 nrd=0.6905 nrs=0.6905 sa=0 sb=0 sd=0 mult=8 m=8
XMgn6p vcl dac6 gon6 vss sky130_fd_pr__nfet_g5v0d10v5 L=0.5 W=0.84 nf=1 ad=0.2436 as=0.2436 pd=2.26
+ ps=2.26 nrd=0.3452 nrs=0.3452 sa=0 sb=0 sd=0 mult=1 m=1
XMgn6n gon6 dacb6 vss vss sky130_fd_pr__nfet_g5v0d10v5 L=0.5 W=0.84 nf=1 ad=0.2436 as=0.2436 pd=2.26
+ ps=2.26 nrd=0.3452 nrs=0.3452 sa=0 sb=0 sd=0 mult=1 m=1
XMgf6p vcl dacb6 gof6 vss sky130_fd_pr__nfet_g5v0d10v5 L=0.5 W=0.84 nf=1 ad=0.2436 as=0.2436 pd=2.26
+ ps=2.26 nrd=0.3452 nrs=0.3452 sa=0 sb=0 sd=0 mult=1 m=1
XMgf6n gof6 dac6 vss vss sky130_fd_pr__nfet_g5v0d10v5 L=0.5 W=0.84 nf=1 ad=0.2436 as=0.2436 pd=2.26
+ ps=2.26 nrd=0.3452 nrs=0.3452 sa=0 sb=0 sd=0 mult=1 m=1
XMu6 sk6 ndac vss vss sky130_fd_pr__nfet_g5v0d10v5 L=2 W=4.68 nf=1 ad=1.357 as=1.357 pd=9.94 ps=9.94
+ nrd=0.06197 nrs=0.06197 sa=0 sb=0 sd=0 mult=64 m=64
XMdi7p dacb7 dac7 vdd vdd sky130_fd_pr__pfet_g5v0d10v5 L=0.5 W=0.84 nf=1 ad=0.2436 as=0.2436 pd=2.26
+ ps=2.26 nrd=0.3452 nrs=0.3452 sa=0 sb=0 sd=0 mult=1 m=1
XMdi7n dacb7 dac7 vss vss sky130_fd_pr__nfet_g5v0d10v5 L=0.5 W=0.84 nf=1 ad=0.2436 as=0.2436 pd=2.26
+ ps=2.26 nrd=0.3452 nrs=0.3452 sa=0 sb=0 sd=0 mult=1 m=1
XMon7 int gon7 sk7 vss sky130_fd_pr__nfet_g5v0d10v5 L=1 W=0.42 nf=1 ad=0.1218 as=0.1218 pd=1.42
+ ps=1.42 nrd=0.6905 nrs=0.6905 sa=0 sb=0 sd=0 mult=16 m=16
XMof7 vdd gof7 sk7 vss sky130_fd_pr__nfet_g5v0d10v5 L=1 W=0.42 nf=1 ad=0.1218 as=0.1218 pd=1.42
+ ps=1.42 nrd=0.6905 nrs=0.6905 sa=0 sb=0 sd=0 mult=16 m=16
XMgn7p vcl dac7 gon7 vss sky130_fd_pr__nfet_g5v0d10v5 L=0.5 W=0.84 nf=1 ad=0.2436 as=0.2436 pd=2.26
+ ps=2.26 nrd=0.3452 nrs=0.3452 sa=0 sb=0 sd=0 mult=1 m=1
XMgn7n gon7 dacb7 vss vss sky130_fd_pr__nfet_g5v0d10v5 L=0.5 W=0.84 nf=1 ad=0.2436 as=0.2436 pd=2.26
+ ps=2.26 nrd=0.3452 nrs=0.3452 sa=0 sb=0 sd=0 mult=1 m=1
XMgf7p vcl dacb7 gof7 vss sky130_fd_pr__nfet_g5v0d10v5 L=0.5 W=0.84 nf=1 ad=0.2436 as=0.2436 pd=2.26
+ ps=2.26 nrd=0.3452 nrs=0.3452 sa=0 sb=0 sd=0 mult=1 m=1
XMgf7n gof7 dac7 vss vss sky130_fd_pr__nfet_g5v0d10v5 L=0.5 W=0.84 nf=1 ad=0.2436 as=0.2436 pd=2.26
+ ps=2.26 nrd=0.3452 nrs=0.3452 sa=0 sb=0 sd=0 mult=1 m=1
XMu7 sk7 ndac vss vss sky130_fd_pr__nfet_g5v0d10v5 L=2 W=4.68 nf=1 ad=1.357 as=1.357 pd=9.94 ps=9.94
+ nrd=0.06197 nrs=0.06197 sa=0 sb=0 sd=0 mult=128 m=128
XMtl tl adc_lat vss vss sky130_fd_pr__nfet_g5v0d10v5 L=0.5 W=0.57 nf=1 ad=0.1653 as=0.1653 pd=1.72
+ ps=1.72 nrd=0.5088 nrs=0.5088 sa=0 sb=0 sd=0 mult=2 m=2
XM1a xa int tl vss sky130_fd_pr__nfet_g5v0d10v5 L=1 W=4.21 nf=1 ad=1.221 as=1.221 pd=9 ps=9
+ nrd=0.06888 nrs=0.06888 sa=0 sb=0 sd=0 mult=1 m=1
XM1b xb intr tl vss sky130_fd_pr__nfet_g5v0d10v5 L=1 W=4.21 nf=1 ad=1.221 as=1.221 pd=9 ps=9
+ nrd=0.06888 nrs=0.06888 sa=0 sb=0 sd=0 mult=1 m=1
XM2a oa ob xa vss sky130_fd_pr__nfet_g5v0d10v5 L=0.5 W=0.57 nf=1 ad=0.1653 as=0.1653 pd=1.72 ps=1.72
+ nrd=0.5088 nrs=0.5088 sa=0 sb=0 sd=0 mult=1 m=1
XM2b ob oa xb vss sky130_fd_pr__nfet_g5v0d10v5 L=0.5 W=0.57 nf=1 ad=0.1653 as=0.1653 pd=1.72 ps=1.72
+ nrd=0.5088 nrs=0.5088 sa=0 sb=0 sd=0 mult=1 m=1
XM3a oa ob vdd vdd sky130_fd_pr__pfet_g5v0d10v5 L=0.5 W=0.57 nf=1 ad=0.1653 as=0.1653 pd=1.72
+ ps=1.72 nrd=0.5088 nrs=0.5088 sa=0 sb=0 sd=0 mult=1 m=1
XM3b ob oa vdd vdd sky130_fd_pr__pfet_g5v0d10v5 L=0.5 W=0.57 nf=1 ad=0.1653 as=0.1653 pd=1.72
+ ps=1.72 nrd=0.5088 nrs=0.5088 sa=0 sb=0 sd=0 mult=1 m=1
XMra oa adc_lat vdd vdd sky130_fd_pr__pfet_g5v0d10v5 L=0.5 W=0.84 nf=1 ad=0.2436 as=0.2436 pd=2.26
+ ps=2.26 nrd=0.3452 nrs=0.3452 sa=0 sb=0 sd=0 mult=1 m=1
XMrb ob adc_lat vdd vdd sky130_fd_pr__pfet_g5v0d10v5 L=0.5 W=0.84 nf=1 ad=0.2436 as=0.2436 pd=2.26
+ ps=2.26 nrd=0.3452 nrs=0.3452 sa=0 sb=0 sd=0 mult=1 m=1
XMrxa xa adc_lat vdd vdd sky130_fd_pr__pfet_g5v0d10v5 L=0.5 W=0.84 nf=1 ad=0.2436 as=0.2436 pd=2.26
+ ps=2.26 nrd=0.3452 nrs=0.3452 sa=0 sb=0 sd=0 mult=1 m=1
XMrxb xb adc_lat vdd vdd sky130_fd_pr__pfet_g5v0d10v5 L=0.5 W=0.84 nf=1 ad=0.2436 as=0.2436 pd=2.26
+ ps=2.26 nrd=0.3452 nrs=0.3452 sa=0 sb=0 sd=0 mult=1 m=1
XMp_cmpa cmp oa vdd vdd sky130_fd_pr__pfet_g5v0d10v5 L=0.5 W=0.84 nf=1 ad=0.2436 as=0.2436 pd=2.26
+ ps=2.26 nrd=0.3452 nrs=0.3452 sa=0 sb=0 sd=0 mult=1 m=1
XMp_cmpb cmp cmpb vdd vdd sky130_fd_pr__pfet_g5v0d10v5 L=0.5 W=0.84 nf=1 ad=0.2436 as=0.2436 pd=2.26
+ ps=2.26 nrd=0.3452 nrs=0.3452 sa=0 sb=0 sd=0 mult=1 m=1
XMn_cmpa cmp oa n_cmp vss sky130_fd_pr__nfet_g5v0d10v5 L=0.5 W=0.84 nf=1 ad=0.2436 as=0.2436 pd=2.26
+ ps=2.26 nrd=0.3452 nrs=0.3452 sa=0 sb=0 sd=0 mult=1 m=1
XMn_cmpb n_cmp cmpb vss vss sky130_fd_pr__nfet_g5v0d10v5 L=0.5 W=0.84 nf=1 ad=0.2436 as=0.2436
+ pd=2.26 ps=2.26 nrd=0.3452 nrs=0.3452 sa=0 sb=0 sd=0 mult=1 m=1
XMp_cmpba cmpb ob vdd vdd sky130_fd_pr__pfet_g5v0d10v5 L=0.5 W=0.84 nf=1 ad=0.2436 as=0.2436 pd=2.26
+ ps=2.26 nrd=0.3452 nrs=0.3452 sa=0 sb=0 sd=0 mult=1 m=1
XMp_cmpbb cmpb cmp vdd vdd sky130_fd_pr__pfet_g5v0d10v5 L=0.5 W=0.84 nf=1 ad=0.2436 as=0.2436
+ pd=2.26 ps=2.26 nrd=0.3452 nrs=0.3452 sa=0 sb=0 sd=0 mult=1 m=1
XMn_cmpba cmpb ob n_cmpb vss sky130_fd_pr__nfet_g5v0d10v5 L=0.5 W=0.84 nf=1 ad=0.2436 as=0.2436
+ pd=2.26 ps=2.26 nrd=0.3452 nrs=0.3452 sa=0 sb=0 sd=0 mult=1 m=1
XMn_cmpbb n_cmpb cmp vss vss sky130_fd_pr__nfet_g5v0d10v5 L=0.5 W=0.84 nf=1 ad=0.2436 as=0.2436
+ pd=2.26 ps=2.26 nrd=0.3452 nrs=0.3452 sa=0 sb=0 sd=0 mult=1 m=1
**.ends
.GLOBAL vdd
.GLOBAL vss
.end
